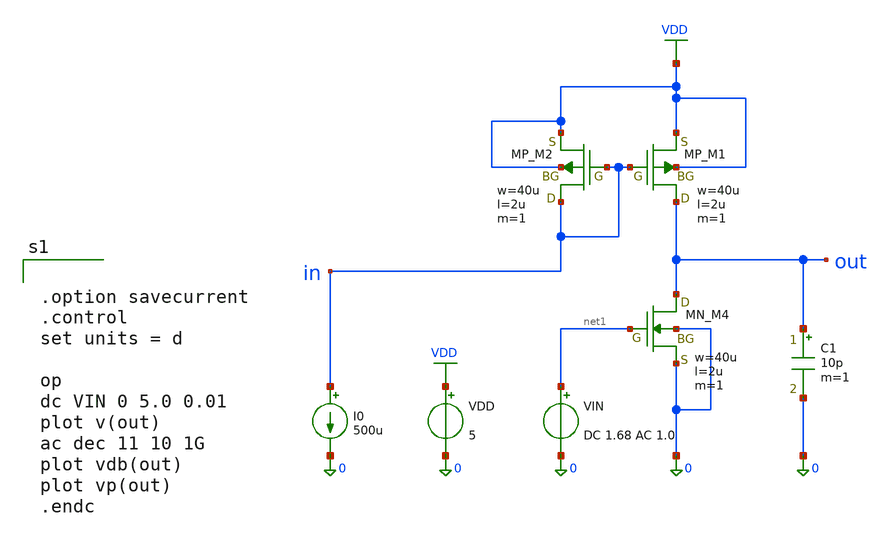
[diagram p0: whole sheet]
** sch_path: member_project/JJY_Receiver/Masahiro/jjy_recv/cmamp/cmamp.sch
**.subckt cmamp
M4 out net1 0 0 NMOS w=40u l=2u as=0 ad=0 ps=0 pd=0 nrd=0 nrs=0 m=1
XM1 out in VDD VDD PMOS w=40u l=2u as=0 ad=0 ps=0 pd=0 nrd=0 nrs=0 m=1
VDD VDD 0 5
VIN net1 0 DC 1.68 AC 1.0
XM2 in in VDD VDD PMOS w=40u l=2u as=0 ad=0 ps=0 pd=0 nrd=0 nrs=0 m=1
I0 in 0 500u
C1 out 0 10p m=1
**** begin user architecture code
 .include $::LIB/ip62_models


.option savecurrent
.control
set units = d

op
dc VIN 0 5.0 0.01
plot v(out)
ac dec 11 10 1G
plot vdb(out)
plot vp(out)
.endc


**** end user architecture code
**.ends
.GLOBAL VDD
.end
